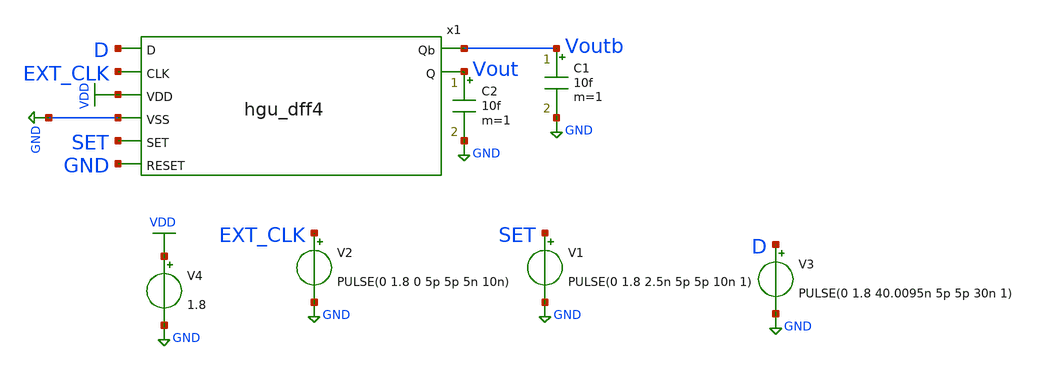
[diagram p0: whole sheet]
** sch_path: hgu/tb/tb_hgu_dff4.sch
**.subckt tb_hgu_dff4
V2 EXT_CLK GND PULSE(0 1.8 0 5p 5p 5n 10n)
C1 Voutb GND 10f m=1
x1 D Voutb Vout EXT_CLK VDD GND SET GND hgu_dff4
C2 Vout GND 10f m=1
V1 SET GND PULSE(0 1.8 2.5n 5p 5p 10n 1)
V3 D GND PULSE(0 1.8 40.0095n 5p 5p 30n 1)
V4 VDD GND 1.8
**** begin user architecture code



.lib /foss/pdks/sky130A/libs.tech/ngspice/sky130.lib.spice tt

.dc VDD 1.8 1.8
.dc GND 0 0

.tran 1ps 60ns

.control
	run
	plot V(D) V(Vout) V(SET) V(EXT_CLK)
.endc
.save all



**** end user architecture code
**.ends

* expanding   symbol:  ../xschem/hgu_dff4.sym # of pins=8
** sym_path: xschem/hgu_dff4.sym
** sch_path: xschem/hgu_dff4.sch
.subckt hgu_dff4 D Qb Q CLK VDD VSS SET RESET
*.ipin CLK
*.ipin VDD
*.ipin VSS
*.ipin SET
*.ipin RESET
*.ipin D
*.opin Qb
*.opin Q
x27 CLK D net1 net2 VGND VNB VPB VPWR Q Qb sky130_fd_sc_hd__dfbbp_1
x4 SET VGND VNB VPB VPWR net2 sky130_fd_sc_hd__inv_1
x5 RESET VGND VNB VPB VPWR net1 sky130_fd_sc_hd__inv_1
.ends

.GLOBAL VDD
.GLOBAL GND
.end
